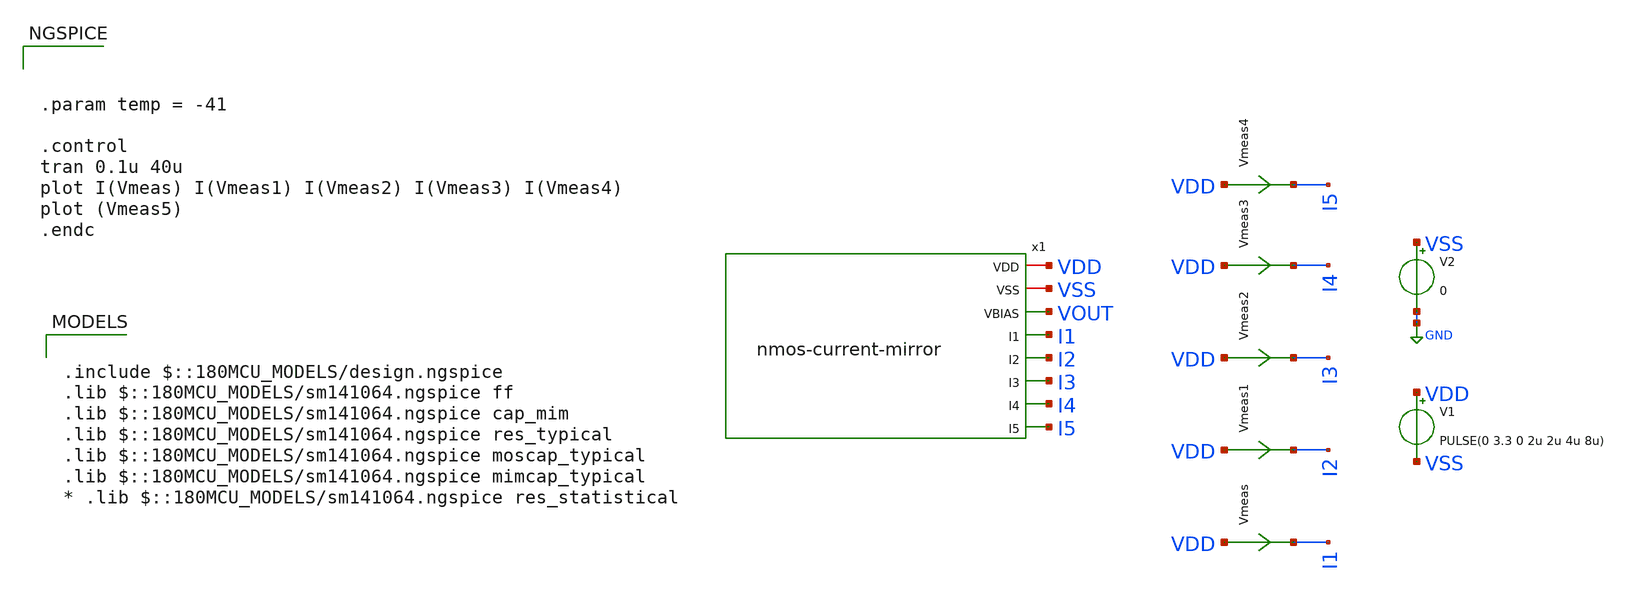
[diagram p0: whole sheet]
** sch_path: w1_advanced-foundation/w1_task/w1_tb/tb_current-mirror.sch
**.subckt tb_current-mirror
V1 VDD VSS PULSE(0 3.3 0 2u 2u 4u 8u)
V2 VSS GND 0
Vmeas VDD I1 0
.save i(vmeas)
Vmeas1 VDD I2 0
.save i(vmeas1)
Vmeas2 VDD I3 0
.save i(vmeas2)
Vmeas3 VDD I4 0
.save i(vmeas3)
Vmeas4 VDD I5 0
.save i(vmeas4)
x1 VDD VSS VOUT I1 I2 I3 I4 I5 nmos-current-mirror
**** begin user architecture code

.include $::180MCU_MODELS/design.ngspice
.lib $::180MCU_MODELS/sm141064.ngspice ff
.lib $::180MCU_MODELS/sm141064.ngspice cap_mim
.lib $::180MCU_MODELS/sm141064.ngspice res_typical
.lib $::180MCU_MODELS/sm141064.ngspice moscap_typical
.lib $::180MCU_MODELS/sm141064.ngspice mimcap_typical
* .lib $::180MCU_MODELS/sm141064.ngspice res_statistical




.param temp = -41

.control
tran 0.1u 40u
plot I(Vmeas) I(Vmeas1) I(Vmeas2) I(Vmeas3) I(Vmeas4)
plot (Vmeas5)
.endc


**** end user architecture code
**.ends

* expanding   symbol:
*+  /foss/designs/aic-sems-v/w1_advanced-foundation/w1_task/w1_current_mirror/nmos-current-mirror.sym # of pins=8
** sym_path: w1_advanced-foundation/w1_task/w1_current_mirror/nmos-current-mirror.sym
** sch_path: w1_advanced-foundation/w1_task/w1_current_mirror/nmos-current-mirror.sch
.subckt nmos-current-mirror VDD VSS VBIAS I1 I2 I5 I3 I4
*.opin I4
*.opin I3
*.opin I1
*.opin I2
*.opin I5
*.iopin VDD
*.iopin VSS
*.opin VBIAS
XM1 I1 VBIAS VSS VSS nfet_03v3 L=2u W=37.5u nf=1 ad='int((nf+1)/2) * W/nf * 0.18u' as='int((nf+2)/2) * W/nf * 0.18u'
+ pd='2*int((nf+1)/2) * (W/nf + 0.18u)' ps='2*int((nf+2)/2) * (W/nf + 0.18u)' nrd='0.18u / W' nrs='0.18u / W'
+ sa=0 sb=0 sd=0 m=1
XM2 I2 VBIAS VSS VSS nfet_03v3 L=2u W=37.5u nf=1 ad='int((nf+1)/2) * W/nf * 0.18u' as='int((nf+2)/2) * W/nf * 0.18u'
+ pd='2*int((nf+1)/2) * (W/nf + 0.18u)' ps='2*int((nf+2)/2) * (W/nf + 0.18u)' nrd='0.18u / W' nrs='0.18u / W'
+ sa=0 sb=0 sd=0 m=2
XM3 I3 VBIAS VSS VSS nfet_03v3 L=2u W=37.5u nf=1 ad='int((nf+1)/2) * W/nf * 0.18u' as='int((nf+2)/2) * W/nf * 0.18u'
+ pd='2*int((nf+1)/2) * (W/nf + 0.18u)' ps='2*int((nf+2)/2) * (W/nf + 0.18u)' nrd='0.18u / W' nrs='0.18u / W'
+ sa=0 sb=0 sd=0 m=3
XM4 I4 VBIAS VSS VSS nfet_03v3 L=2u W=37.5u nf=1 ad='int((nf+1)/2) * W/nf * 0.18u' as='int((nf+2)/2) * W/nf * 0.18u'
+ pd='2*int((nf+1)/2) * (W/nf + 0.18u)' ps='2*int((nf+2)/2) * (W/nf + 0.18u)' nrd='0.18u / W' nrs='0.18u / W'
+ sa=0 sb=0 sd=0 m=4
XM5 I5 VBIAS VSS VSS nfet_03v3 L=2u W=37.5u nf=1 ad='int((nf+1)/2) * W/nf * 0.18u' as='int((nf+2)/2) * W/nf * 0.18u'
+ pd='2*int((nf+1)/2) * (W/nf + 0.18u)' ps='2*int((nf+2)/2) * (W/nf + 0.18u)' nrd='0.18u / W' nrs='0.18u / W'
+ sa=0 sb=0 sd=0 m=5
x1 VDD VSS VBIAS n-bias-gen
.ends


* expanding   symbol:
*+  /foss/designs/aic-sems-v/w1_advanced-foundation/w1_task/w1_current_mirror/n-bias-gen.sym # of pins=3
** sym_path: w1_advanced-foundation/w1_task/w1_current_mirror/n-bias-gen.sym
** sch_path: w1_advanced-foundation/w1_task/w1_current_mirror/n-bias-gen.sch
.subckt n-bias-gen VDD VSS VBIAS
*.iopin VDD
*.iopin VSS
*.opin VBIAS
XM1 VBIAS VBIAS VSS VSS nfet_03v3 L=2u W=37.5u nf=1 ad='int((nf+1)/2) * W/nf * 0.18u' as='int((nf+2)/2) * W/nf * 0.18u'
+ pd='2*int((nf+1)/2) * (W/nf + 0.18u)' ps='2*int((nf+2)/2) * (W/nf + 0.18u)' nrd='0.18u / W' nrs='0.18u / W'
+ sa=0 sb=0 sd=0 m=1
XR1 VBIAS net9 VSS ppolyf_u_1k r_width=4e-6 r_length=100e-6 m=1
XR2 net1 VDD VSS ppolyf_u_1k r_width=4e-6 r_length=100e-6 m=1
XR3 net2 net1 VSS ppolyf_u_1k r_width=4e-6 r_length=100e-6 m=1
XR4 net9 net8 VSS ppolyf_u_1k r_width=4e-6 r_length=100e-6 m=1
XR5 net3 net2 VSS ppolyf_u_1k r_width=4e-6 r_length=100e-6 m=1
XR6 net8 net7 VSS ppolyf_u_1k r_width=4e-6 r_length=100e-6 m=1
XR7 net4 net3 VSS ppolyf_u_1k r_width=4e-6 r_length=100e-6 m=1
XR8 net7 net6 VSS ppolyf_u_1k r_width=4e-6 r_length=100e-6 m=1
XR9 net5 net4 VSS ppolyf_u_1k r_width=4e-6 r_length=100e-6 m=1
XR10 net6 net5 VSS ppolyf_u_1k r_width=4e-6 r_length=100e-6 m=1
.ends

.GLOBAL GND
.end
